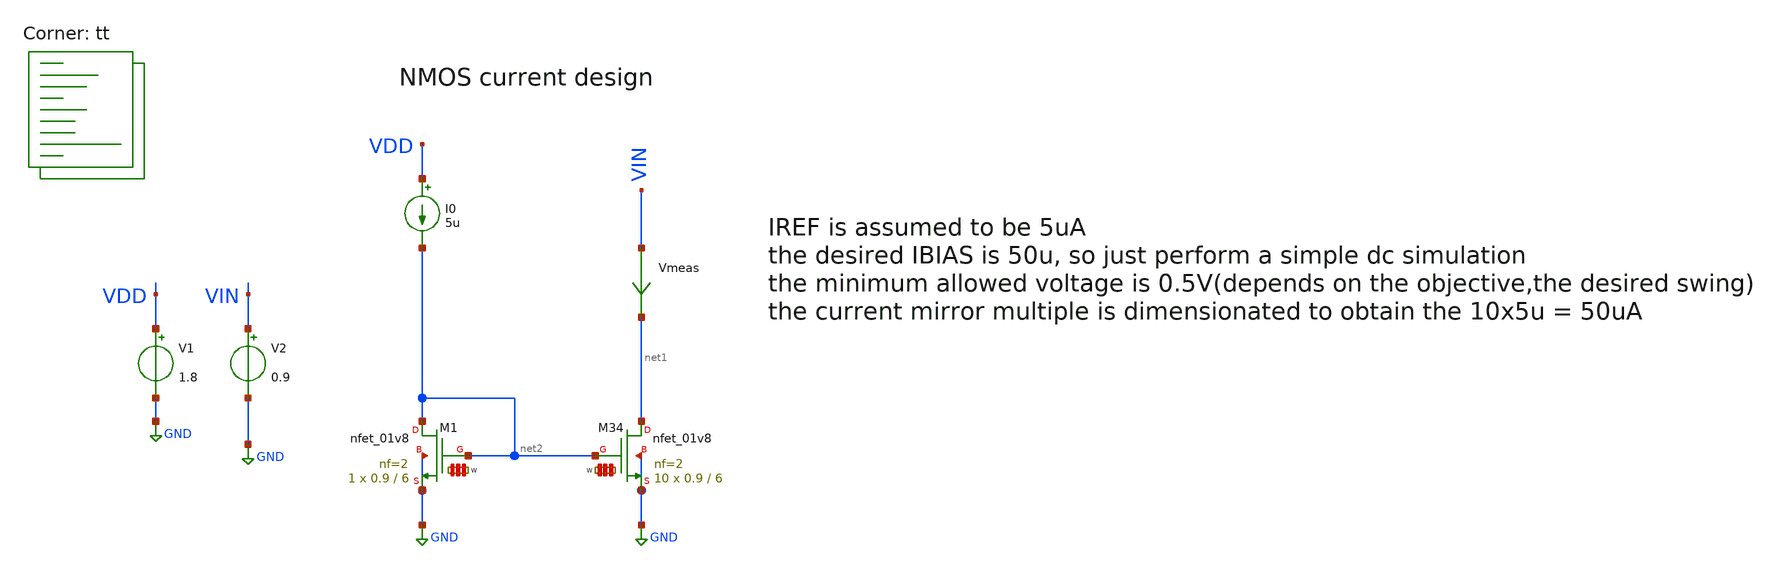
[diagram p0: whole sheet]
** sch_path: my_ip/sky130A/transimpedance_opa,p_1_v8/current_mirror.sch
**.subckt current_mirror
V1 VDD GND 1.8
V2 VIN GND 0.9
Vmeas VIN net1 0
.save i(vmeas)
I0 VDD net2 5u
XM34 net1 net2 GND GND sky130_fd_pr__nfet_01v8 L=6 W='0.9 * 2 ' nf=2 ad='int((2 + 1)/2) * 0.9 / 2 * 0.29'
+ as='int((2 + 2)/2) * 0.9 / 2 * 0.29' pd='2*int((2 + 1)/2) * (0.9 / 2 + 0.29)' ps='2*int((2 + 2)/2) * (0.9 / 2 + 0.29)'
+ nrd='0.29 / 0.9 ' nrs='0.29 / 0.9 ' sa=0 sb=0 sd=0 mult=10 m=10
XM1 net2 net2 GND GND sky130_fd_pr__nfet_01v8 L=6 W='0.9 * 2 ' nf=2 ad='int((2 + 1)/2) * 0.9 / 2 * 0.29'
+ as='int((2 + 2)/2) * 0.9 / 2 * 0.29' pd='2*int((2 + 1)/2) * (0.9 / 2 + 0.29)' ps='2*int((2 + 2)/2) * (0.9 / 2 + 0.29)'
+ nrd='0.29 / 0.9 ' nrs='0.29 / 0.9 ' sa=0 sb=0 sd=0 mult=1 m=1
**** begin user architecture code
.lib $::SKYWATER_MODELS/sky130.lib.spice tt

**************************************************************
**************************************************************
**************************************************************
**************************************************************
**************************************************************
*LIBs*********************************************************
**************************************************************
**************************************************************
**************************************************************
**************************************************************
**************************************************************
*.lib $::SKYWATER_MODELS/sky130.lib.spice tt
* chose the corners in the corner file
* tt_mm for mismatch
* ss ff sf fs standart corners
* ll hh lh hl capacitor and resistors corners
* mc for total process variation including corners
**************************************************************
**************************************************************
**************************************************************
**************************************************************
**************************************************************
*Corners/montecarlo options***********************************
**************************************************************
**************************************************************
**************************************************************
**************************************************************
**************************************************************
.TEMP 27
**************************************************************
**************************************************************
**************************************************************
**************************************************************
*SIMULATION and Plots*****************************************
**************************************************************
**************************************************************
**************************************************************
**************************************************************
.control
save all
dc V2 0 1.8 0.001
*dc simulation
plot i(Vmeas)
plot 1/deriv(i(Vmeas))
.endc

**** end user architecture code
**.ends
.GLOBAL GND
.end
